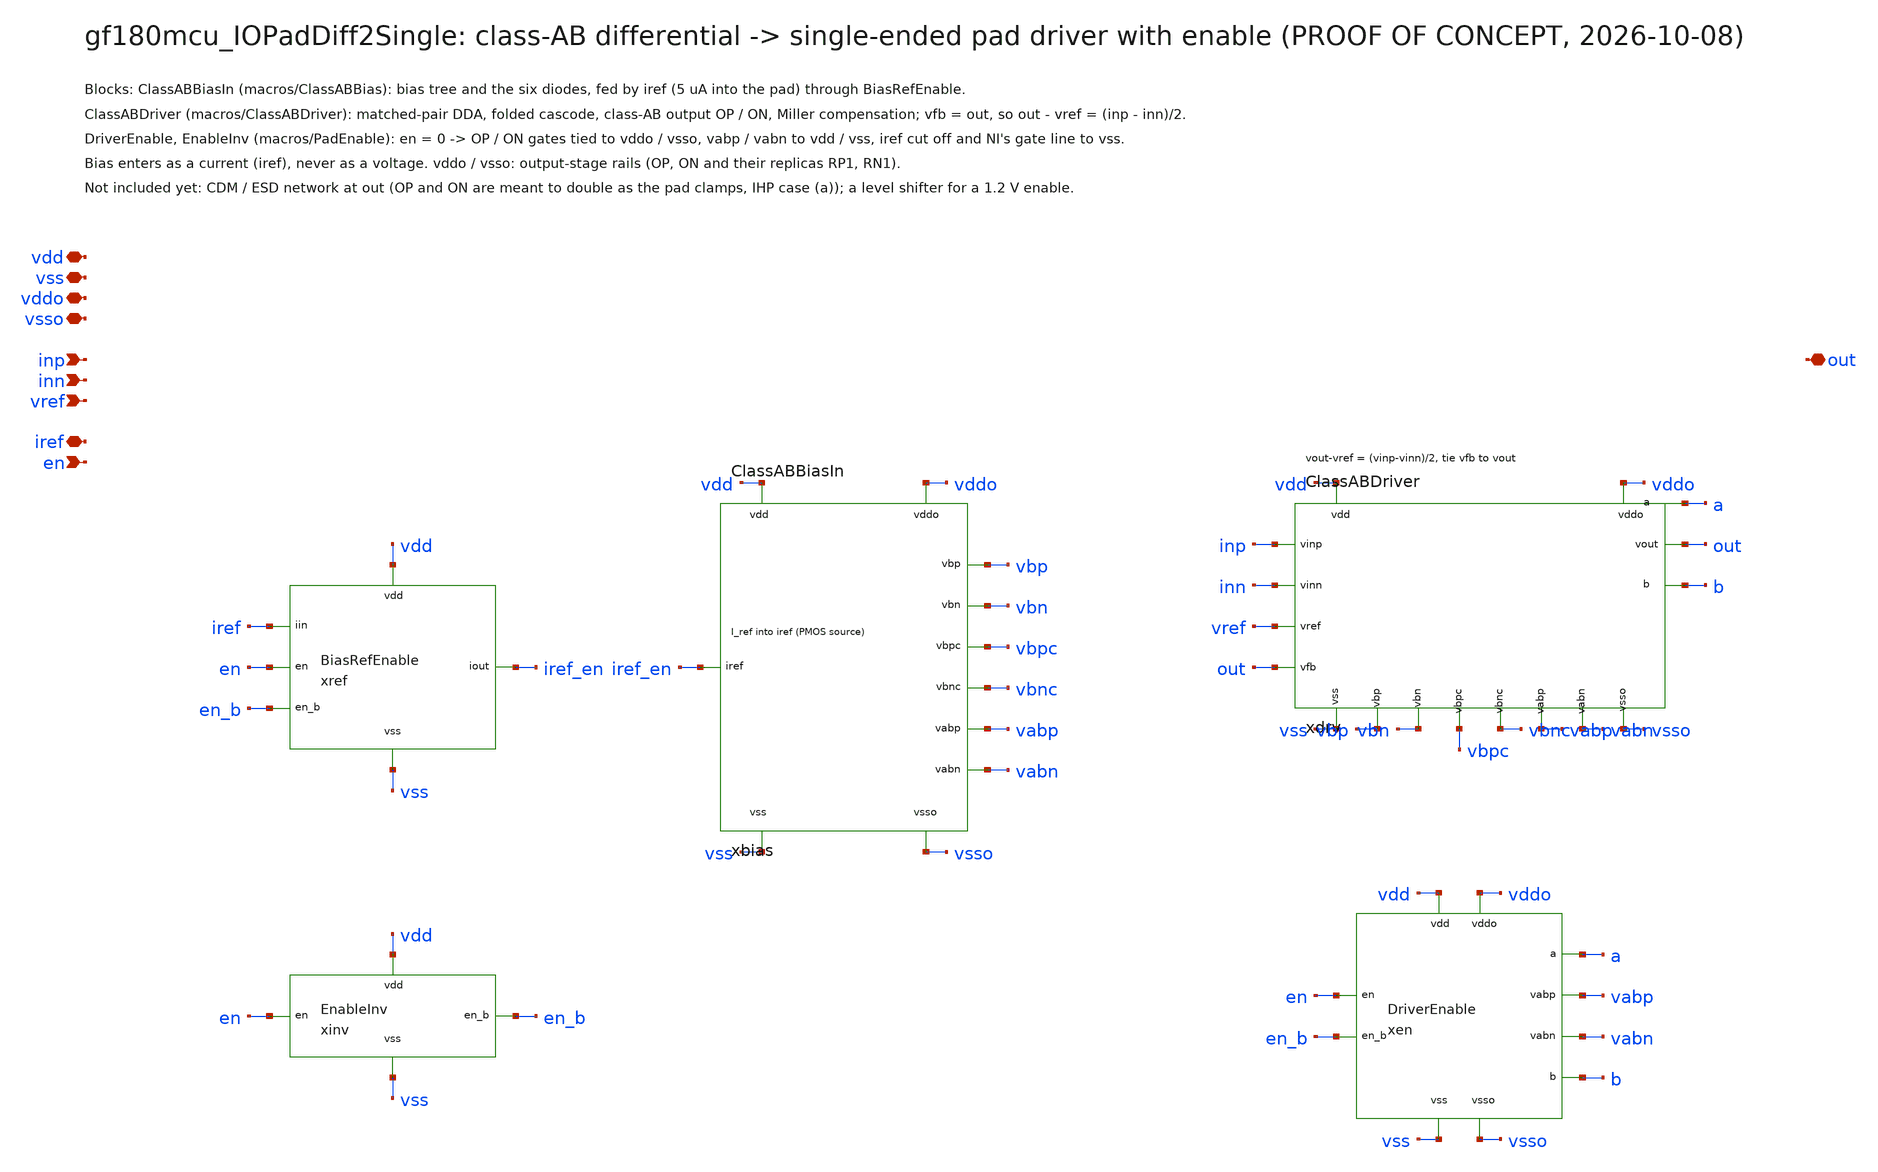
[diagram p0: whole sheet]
** sch_path: macros/gf180mcu_IOPadDiff2Single/schematic/xschem/gf180mcu_IOPadDiff2Single.sch
**.subckt gf180mcu_IOPadDiff2Single vdd vss vddo vsso inp inn vref iref en out
*.iopin vdd
*.iopin vss
*.iopin vddo
*.iopin vsso
*.ipin inp
*.ipin inn
*.ipin vref
*.iopin iref
*.ipin en
*.iopin out
xbias vdd vss vddo vsso iref_en vbp vbn vbpc vbnc vabp vabn ClassABBiasIn
xref vdd vss en en_b iref iref_en BiasRefEnable
xdrv vdd vss vddo vsso inp inn vref out out vbp vbn vbpc vbnc vabp vabn a b ClassABDriver
xen vdd vss vddo vsso en en_b a b vabp vabn DriverEnable
xinv vdd vss en en_b EnableInv
**.ends
.end
